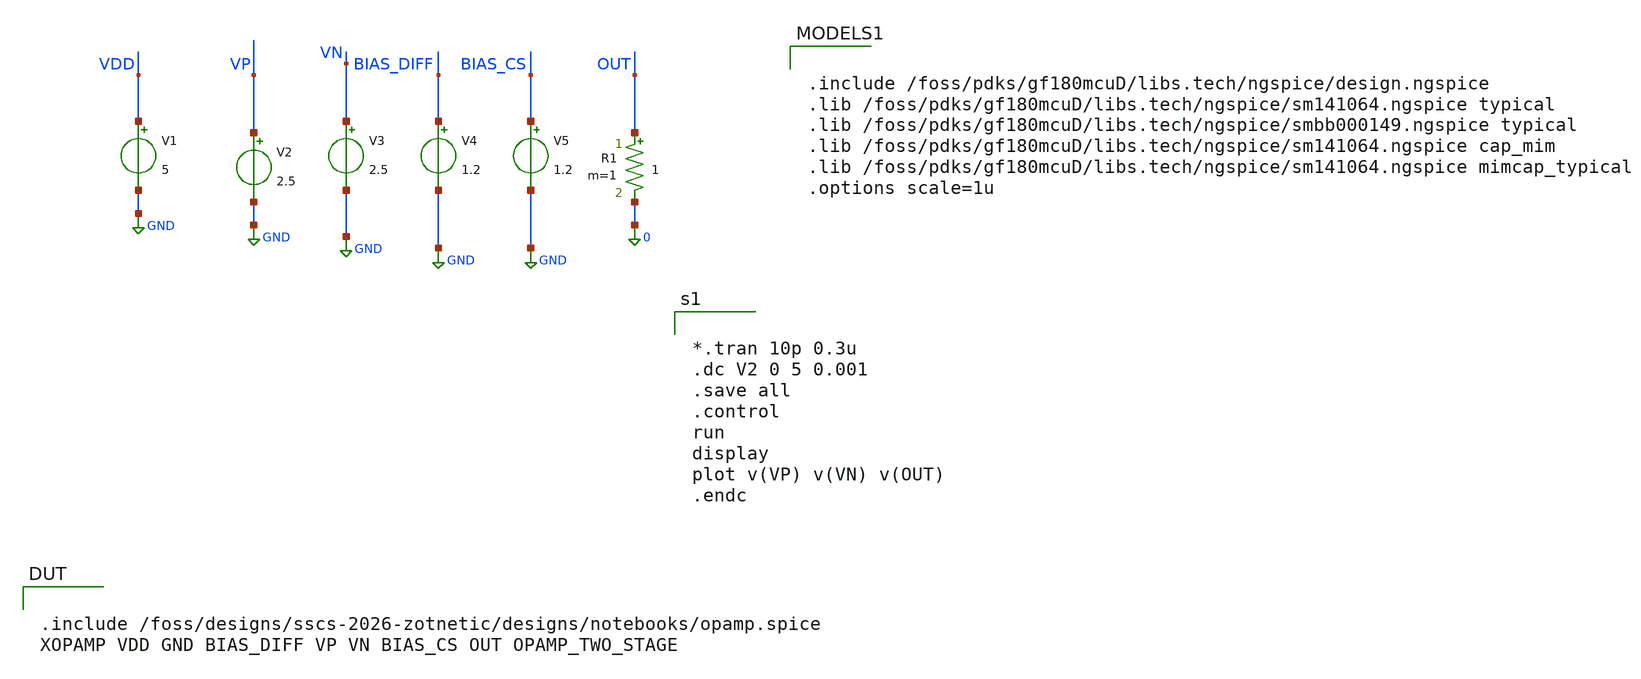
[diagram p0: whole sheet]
** sch_path: designs/notebooks/test2.sch
**.subckt test2
V1 VDD GND 5
V2 VP GND 2.5
V3 VN GND 2.5
V4 BIAS_DIFF GND 1.2
V5 BIAS_CS GND 1.2
R1 OUT 0 1 m=1
**** begin user architecture code


*.tran 10p 0.3u
.dc V2 0 5 0.001
.save all
.control
run
display
plot v(VP) v(VN) v(OUT)
.endc




.include /foss/pdks/gf180mcuD/libs.tech/ngspice/design.ngspice
.lib /foss/pdks/gf180mcuD/libs.tech/ngspice/sm141064.ngspice typical
.lib /foss/pdks/gf180mcuD/libs.tech/ngspice/smbb000149.ngspice typical
.lib /foss/pdks/gf180mcuD/libs.tech/ngspice/sm141064.ngspice cap_mim
.lib /foss/pdks/gf180mcuD/libs.tech/ngspice/sm141064.ngspice mimcap_typical
.options scale=1u



.include /foss/designs/sscs-2026-zotnetic/designs/notebooks/opamp.spice
XOPAMP VDD GND BIAS_DIFF VP VN BIAS_CS OUT OPAMP_TWO_STAGE
**** end user architecture code
**.ends
.GLOBAL GND
.end
